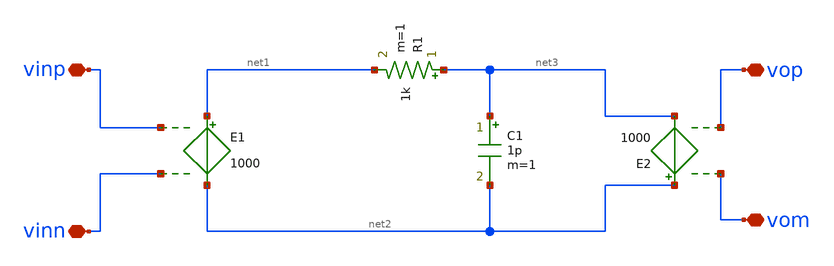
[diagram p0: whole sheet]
** sch_path: xschem/untitled-2.sch
**.subckt untitled-2 vinn vinp vom vop
*.iopin vinn
*.iopin vinp
*.iopin vom
*.iopin vop
E1 net1 net2 vinp vinn 1000
E2 net2 net3 vom vop 1000
R1 net3 net1 1k m=1
C1 net3 net2 1p m=1
**.ends
.end
